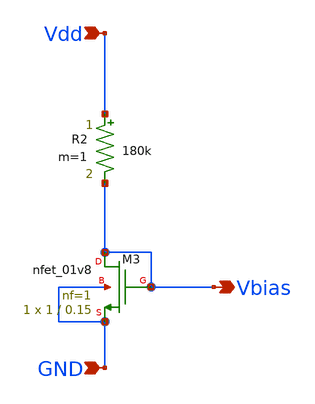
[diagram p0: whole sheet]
** sch_path: current_mirror.sch
**.subckt current_mirror GND Vbias Vdd
*.ipin GND
*.opin Vbias
*.ipin Vdd
R2 Vdd Vbias 180k m=1
XM3 Vbias Vbias GND GND sky130_fd_pr__nfet_01v8 L=0.15 W=1 nf=1 ad='int((1 + 1)/2) * 1 / 1 * 0.29' as='int((1 + 2)/2) * 1 / 1 * 0.29'
+ pd='2*int((1 + 1)/2) * (1 / 1 + 0.29)' ps='2*int((1 + 2)/2) * (1 / 1 + 0.29)' nrd='0.29 / 1 ' nrs='0.29 / 1 '
+ sa=0 sb=0 sd=0 mult=1 m=1
**.ends
.end
